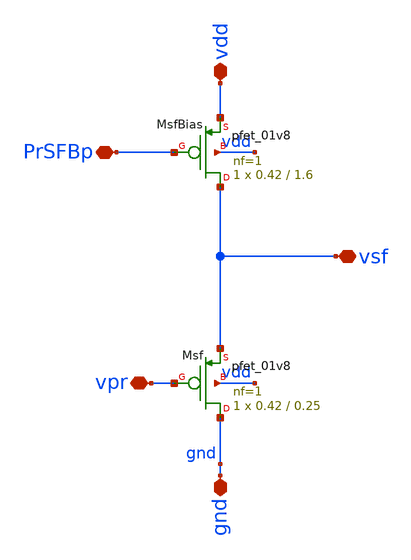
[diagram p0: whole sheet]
** sch_path: analog/xschem/PixelSourceFollower.sch
**.subckt PixelSourceFollower gnd PrSFBp vpr vsf vdd
*.iopin gnd
*.iopin PrSFBp
*.iopin vpr
*.iopin vsf
*.iopin vdd
XMsfBias vsf PrSFBp vdd vdd sky130_fd_pr__pfet_01v8 L=1.6 W=0.42 nf=1 ad='int((1 + 1)/2) * 0.42 / 1 * 0.29'
+ as='int((1 + 2)/2) * 0.42 / 1 * 0.29' pd='2*int((1 + 1)/2) * (0.42 / 1 + 0.29)' ps='2*int((1 + 2)/2) * (0.42 / 1 + 0.29)'
+ nrd='0.29 / 0.42 ' nrs='0.29 / 0.42 ' sa=0 sb=0 sd=0 mult=1 m=1
XMsf gnd vpr vsf vdd sky130_fd_pr__pfet_01v8 L=0.25 W=0.42 nf=1 ad='int((1 + 1)/2) * 0.42 / 1 * 0.29'
+ as='int((1 + 2)/2) * 0.42 / 1 * 0.29' pd='2*int((1 + 1)/2) * (0.42 / 1 + 0.29)' ps='2*int((1 + 2)/2) * (0.42 / 1 + 0.29)'
+ nrd='0.29 / 0.42 ' nrs='0.29 / 0.42 ' sa=0 sb=0 sd=0 mult=1 m=1
**.ends
.end
